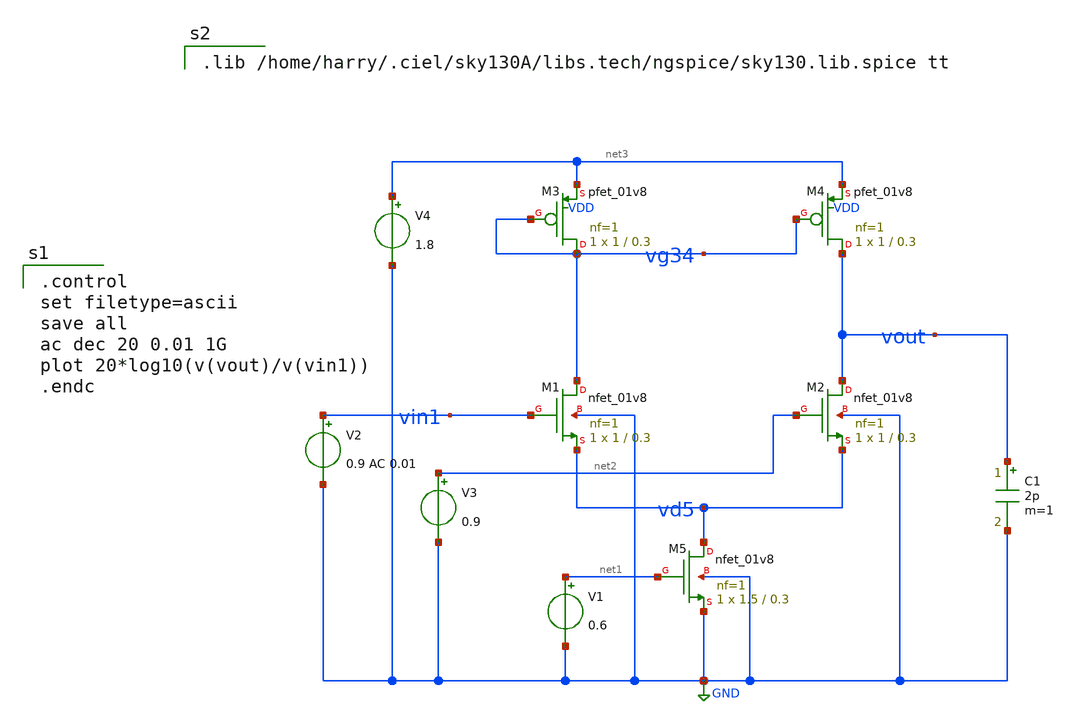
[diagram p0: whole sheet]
** sch_path: magic_xschem_ngspice/DiffAmpMirrorLoad.sch
**.subckt DiffAmpMirrorLoad
XM1 vg34 vin1 vd5 GND sky130_fd_pr__nfet_01v8 L=0.3 W=1 nf=1 ad='int((1 + 1)/2) * 1 / 1 * 0.29' as='int((1 + 2)/2) * 1 / 1 * 0.29'
+ pd='2*int((1 + 1)/2) * (1 / 1 + 0.29)' ps='2*int((1 + 2)/2) * (1 / 1 + 0.29)' nrd='0.29 / 1 ' nrs='0.29 / 1 '
+ sa=0 sb=0 sd=0 mult=1 m=1
XM2 vout net2 vd5 GND sky130_fd_pr__nfet_01v8 L=0.3 W=1 nf=1 ad='int((1 + 1)/2) * 1 / 1 * 0.29' as='int((1 + 2)/2) * 1 / 1 * 0.29'
+ pd='2*int((1 + 1)/2) * (1 / 1 + 0.29)' ps='2*int((1 + 2)/2) * (1 / 1 + 0.29)' nrd='0.29 / 1 ' nrs='0.29 / 1 '
+ sa=0 sb=0 sd=0 mult=1 m=1
XM5 vd5 net1 GND GND sky130_fd_pr__nfet_01v8 L=0.3 W=1.5 nf=1 ad='int((1 + 1)/2) * 1.5 / 1 * 0.29' as='int((1 + 2)/2) * 1.5 / 1 * 0.29'
+ pd='2*int((1 + 1)/2) * (1.5 / 1 + 0.29)' ps='2*int((1 + 2)/2) * (1.5 / 1 + 0.29)' nrd='0.29 / 1.5 ' nrs='0.29 / 1.5 '
+ sa=0 sb=0 sd=0 mult=1 m=1
V1 net1 GND 0.6
V2 vin1 GND 0.9 AC 0.01
V3 net2 GND 0.9
V4 net3 GND 1.8
C1 vout GND 2p m=1
XM3 vg34 vg34 net3 VDD sky130_fd_pr__pfet_01v8 L=0.3 W=1 nf=1 ad='int((1 + 1)/2) * 1 / 1 * 0.29' as='int((1 + 2)/2) * 1 / 1 * 0.29'
+ pd='2*int((1 + 1)/2) * (1 / 1 + 0.29)' ps='2*int((1 + 2)/2) * (1 / 1 + 0.29)' nrd='0.29 / 1 ' nrs='0.29 / 1 '
+ sa=0 sb=0 sd=0 mult=1 m=1
XM4 vout vg34 net3 VDD sky130_fd_pr__pfet_01v8 L=0.3 W=1 nf=1 ad='int((1 + 1)/2) * 1 / 1 * 0.29' as='int((1 + 2)/2) * 1 / 1 * 0.29'
+ pd='2*int((1 + 1)/2) * (1 / 1 + 0.29)' ps='2*int((1 + 2)/2) * (1 / 1 + 0.29)' nrd='0.29 / 1 ' nrs='0.29 / 1 '
+ sa=0 sb=0 sd=0 mult=1 m=1
**** begin user architecture code

.control
set filetype=ascii
save all
ac dec 20 0.01 1G
plot 20*log10(v(vout)/v(vin1))
.endc


.lib /home/harry/.ciel/sky130A/libs.tech/ngspice/sky130.lib.spice tt

**** end user architecture code
**.ends
.GLOBAL GND
.end
